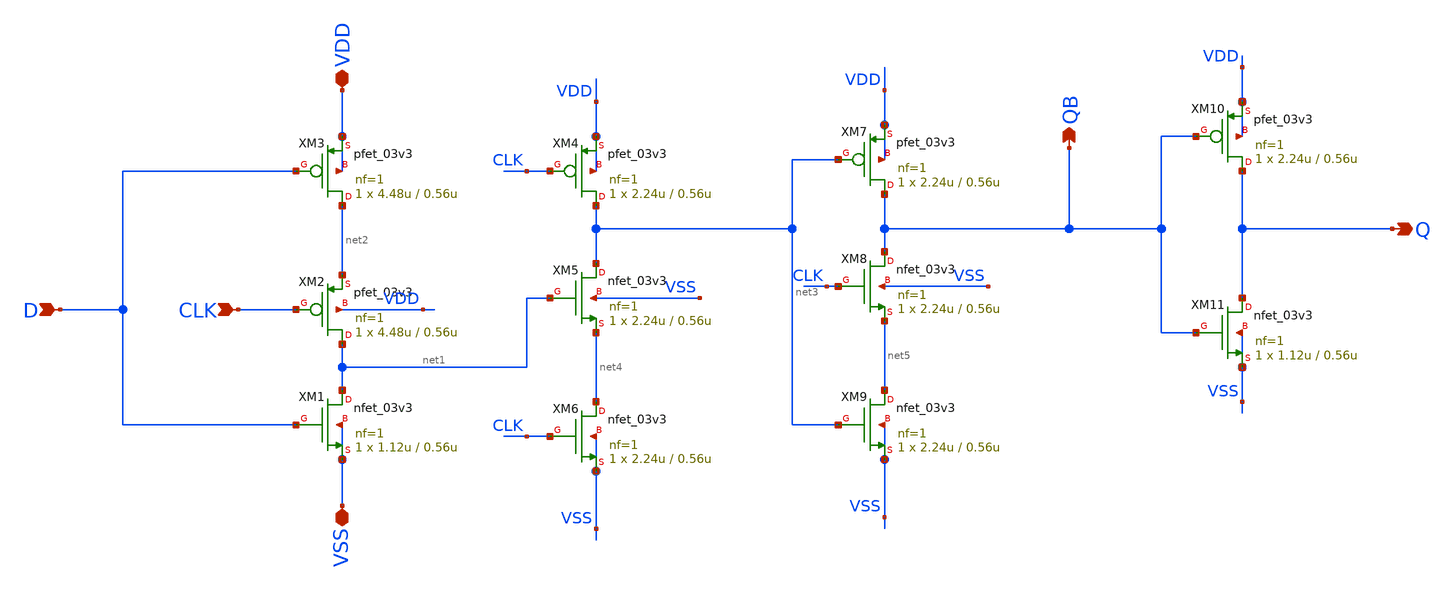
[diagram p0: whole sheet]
** sch_path: PLL-main/schematic/xschem/tspc_FF.sch
**.subckt tspc_FF D CLK VDD VSS QB Q
*.ipin D
*.ipin CLK
*.iopin VDD
*.iopin VSS
*.opin QB
*.opin Q
XM1 net1 D VSS VSS nfet_03v3 L=0.56u W=1.12u nf=1 ad='int((nf+1)/2) * W/nf * 0.18u' as='int((nf+2)/2) * W/nf * 0.18u'
+ pd='2*int((nf+1)/2) * (W/nf + 0.18u)' ps='2*int((nf+2)/2) * (W/nf + 0.18u)' nrd='0.18u / W' nrs='0.18u / W'
+ sa=0 sb=0 sd=0 m=1
XM2 net1 CLK net2 VDD pfet_03v3 L=0.56u W=4.48u nf=1 ad='int((nf+1)/2) * W/nf * 0.18u' as='int((nf+2)/2) * W/nf * 0.18u'
+ pd='2*int((nf+1)/2) * (W/nf + 0.18u)' ps='2*int((nf+2)/2) * (W/nf + 0.18u)' nrd='0.18u / W' nrs='0.18u / W'
+ sa=0 sb=0 sd=0 m=1
XM3 net2 D VDD VDD pfet_03v3 L=0.56u W=4.48u nf=1 ad='int((nf+1)/2) * W/nf * 0.18u' as='int((nf+2)/2) * W/nf * 0.18u'
+ pd='2*int((nf+1)/2) * (W/nf + 0.18u)' ps='2*int((nf+2)/2) * (W/nf + 0.18u)' nrd='0.18u / W' nrs='0.18u / W'
+ sa=0 sb=0 sd=0 m=1
XM4 net3 CLK VDD VDD pfet_03v3 L=0.56u W=2.24u nf=1 ad='int((nf+1)/2) * W/nf * 0.18u' as='int((nf+2)/2) * W/nf * 0.18u'
+ pd='2*int((nf+1)/2) * (W/nf + 0.18u)' ps='2*int((nf+2)/2) * (W/nf + 0.18u)' nrd='0.18u / W' nrs='0.18u / W'
+ sa=0 sb=0 sd=0 m=1
XM5 net3 net1 net4 VSS nfet_03v3 L=0.56u W=2.24u nf=1 ad='int((nf+1)/2) * W/nf * 0.18u' as='int((nf+2)/2) * W/nf * 0.18u'
+ pd='2*int((nf+1)/2) * (W/nf + 0.18u)' ps='2*int((nf+2)/2) * (W/nf + 0.18u)' nrd='0.18u / W' nrs='0.18u / W'
+ sa=0 sb=0 sd=0 m=1
XM6 net4 CLK VSS VSS nfet_03v3 L=0.56u W=2.24u nf=1 ad='int((nf+1)/2) * W/nf * 0.18u' as='int((nf+2)/2) * W/nf * 0.18u'
+ pd='2*int((nf+1)/2) * (W/nf + 0.18u)' ps='2*int((nf+2)/2) * (W/nf + 0.18u)' nrd='0.18u / W' nrs='0.18u / W'
+ sa=0 sb=0 sd=0 m=1
XM7 QB net3 VDD VDD pfet_03v3 L=0.56u W=2.24u nf=1 ad='int((nf+1)/2) * W/nf * 0.18u' as='int((nf+2)/2) * W/nf * 0.18u'
+ pd='2*int((nf+1)/2) * (W/nf + 0.18u)' ps='2*int((nf+2)/2) * (W/nf + 0.18u)' nrd='0.18u / W' nrs='0.18u / W'
+ sa=0 sb=0 sd=0 m=1
XM8 QB CLK net5 VSS nfet_03v3 L=0.56u W=2.24u nf=1 ad='int((nf+1)/2) * W/nf * 0.18u' as='int((nf+2)/2) * W/nf * 0.18u'
+ pd='2*int((nf+1)/2) * (W/nf + 0.18u)' ps='2*int((nf+2)/2) * (W/nf + 0.18u)' nrd='0.18u / W' nrs='0.18u / W'
+ sa=0 sb=0 sd=0 m=1
XM9 net5 net3 VSS VSS nfet_03v3 L=0.56u W=2.24u nf=1 ad='int((nf+1)/2) * W/nf * 0.18u' as='int((nf+2)/2) * W/nf * 0.18u'
+ pd='2*int((nf+1)/2) * (W/nf + 0.18u)' ps='2*int((nf+2)/2) * (W/nf + 0.18u)' nrd='0.18u / W' nrs='0.18u / W'
+ sa=0 sb=0 sd=0 m=1
XM10 Q QB VDD VDD pfet_03v3 L=0.56u W=2.24u nf=1 ad='int((nf+1)/2) * W/nf * 0.18u' as='int((nf+2)/2) * W/nf * 0.18u'
+ pd='2*int((nf+1)/2) * (W/nf + 0.18u)' ps='2*int((nf+2)/2) * (W/nf + 0.18u)' nrd='0.18u / W' nrs='0.18u / W'
+ sa=0 sb=0 sd=0 m=1
XM11 Q QB VSS VSS nfet_03v3 L=0.56u W=1.12u nf=1 ad='int((nf+1)/2) * W/nf * 0.18u' as='int((nf+2)/2) * W/nf * 0.18u'
+ pd='2*int((nf+1)/2) * (W/nf + 0.18u)' ps='2*int((nf+2)/2) * (W/nf + 0.18u)' nrd='0.18u / W' nrs='0.18u / W'
+ sa=0 sb=0 sd=0 m=1
**.ends
.end
